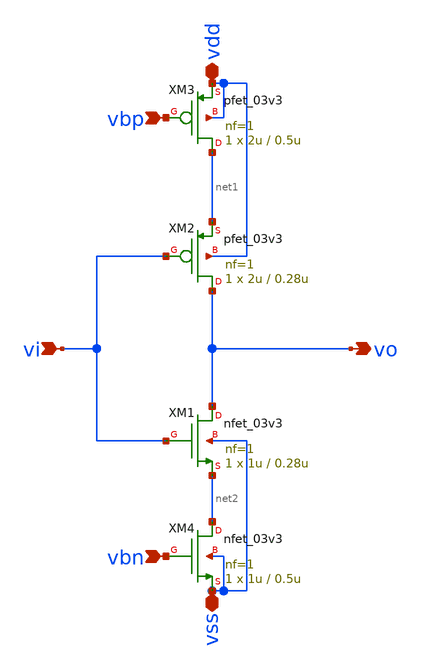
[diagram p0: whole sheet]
** sch_path: src/analog/inv_starved.sch
**.subckt inv_starved vdd vss vi vo vbp vbn
*.iopin vdd
*.iopin vss
*.ipin vi
*.opin vo
*.ipin vbp
*.ipin vbn
XM1 vo vi net2 vss nfet_03v3 L=0.28u W=1u nf=1 ad='int((nf+1)/2) * W/nf * 0.18u' as='int((nf+2)/2) * W/nf * 0.18u'
+ pd='2*int((nf+1)/2) * (W/nf + 0.18u)' ps='2*int((nf+2)/2) * (W/nf + 0.18u)' nrd='0.18u / W' nrs='0.18u / W'
+ sa=0 sb=0 sd=0 m=1
XM2 vo vi net1 vdd pfet_03v3 L=0.28u W=2u nf=1 ad='int((nf+1)/2) * W/nf * 0.18u' as='int((nf+2)/2) * W/nf * 0.18u'
+ pd='2*int((nf+1)/2) * (W/nf + 0.18u)' ps='2*int((nf+2)/2) * (W/nf + 0.18u)' nrd='0.18u / W' nrs='0.18u / W'
+ sa=0 sb=0 sd=0 m=1
XM3 net1 vbp vdd vdd pfet_03v3 L=0.5u W=2u nf=1 ad='int((nf+1)/2) * W/nf * 0.18u' as='int((nf+2)/2) * W/nf * 0.18u'
+ pd='2*int((nf+1)/2) * (W/nf + 0.18u)' ps='2*int((nf+2)/2) * (W/nf + 0.18u)' nrd='0.18u / W' nrs='0.18u / W'
+ sa=0 sb=0 sd=0 m=1
XM4 net2 vbn vss vss nfet_03v3 L=0.5u W=1u nf=1 ad='int((nf+1)/2) * W/nf * 0.18u' as='int((nf+2)/2) * W/nf * 0.18u'
+ pd='2*int((nf+1)/2) * (W/nf + 0.18u)' ps='2*int((nf+2)/2) * (W/nf + 0.18u)' nrd='0.18u / W' nrs='0.18u / W'
+ sa=0 sb=0 sd=0 m=1
**.ends
.end
